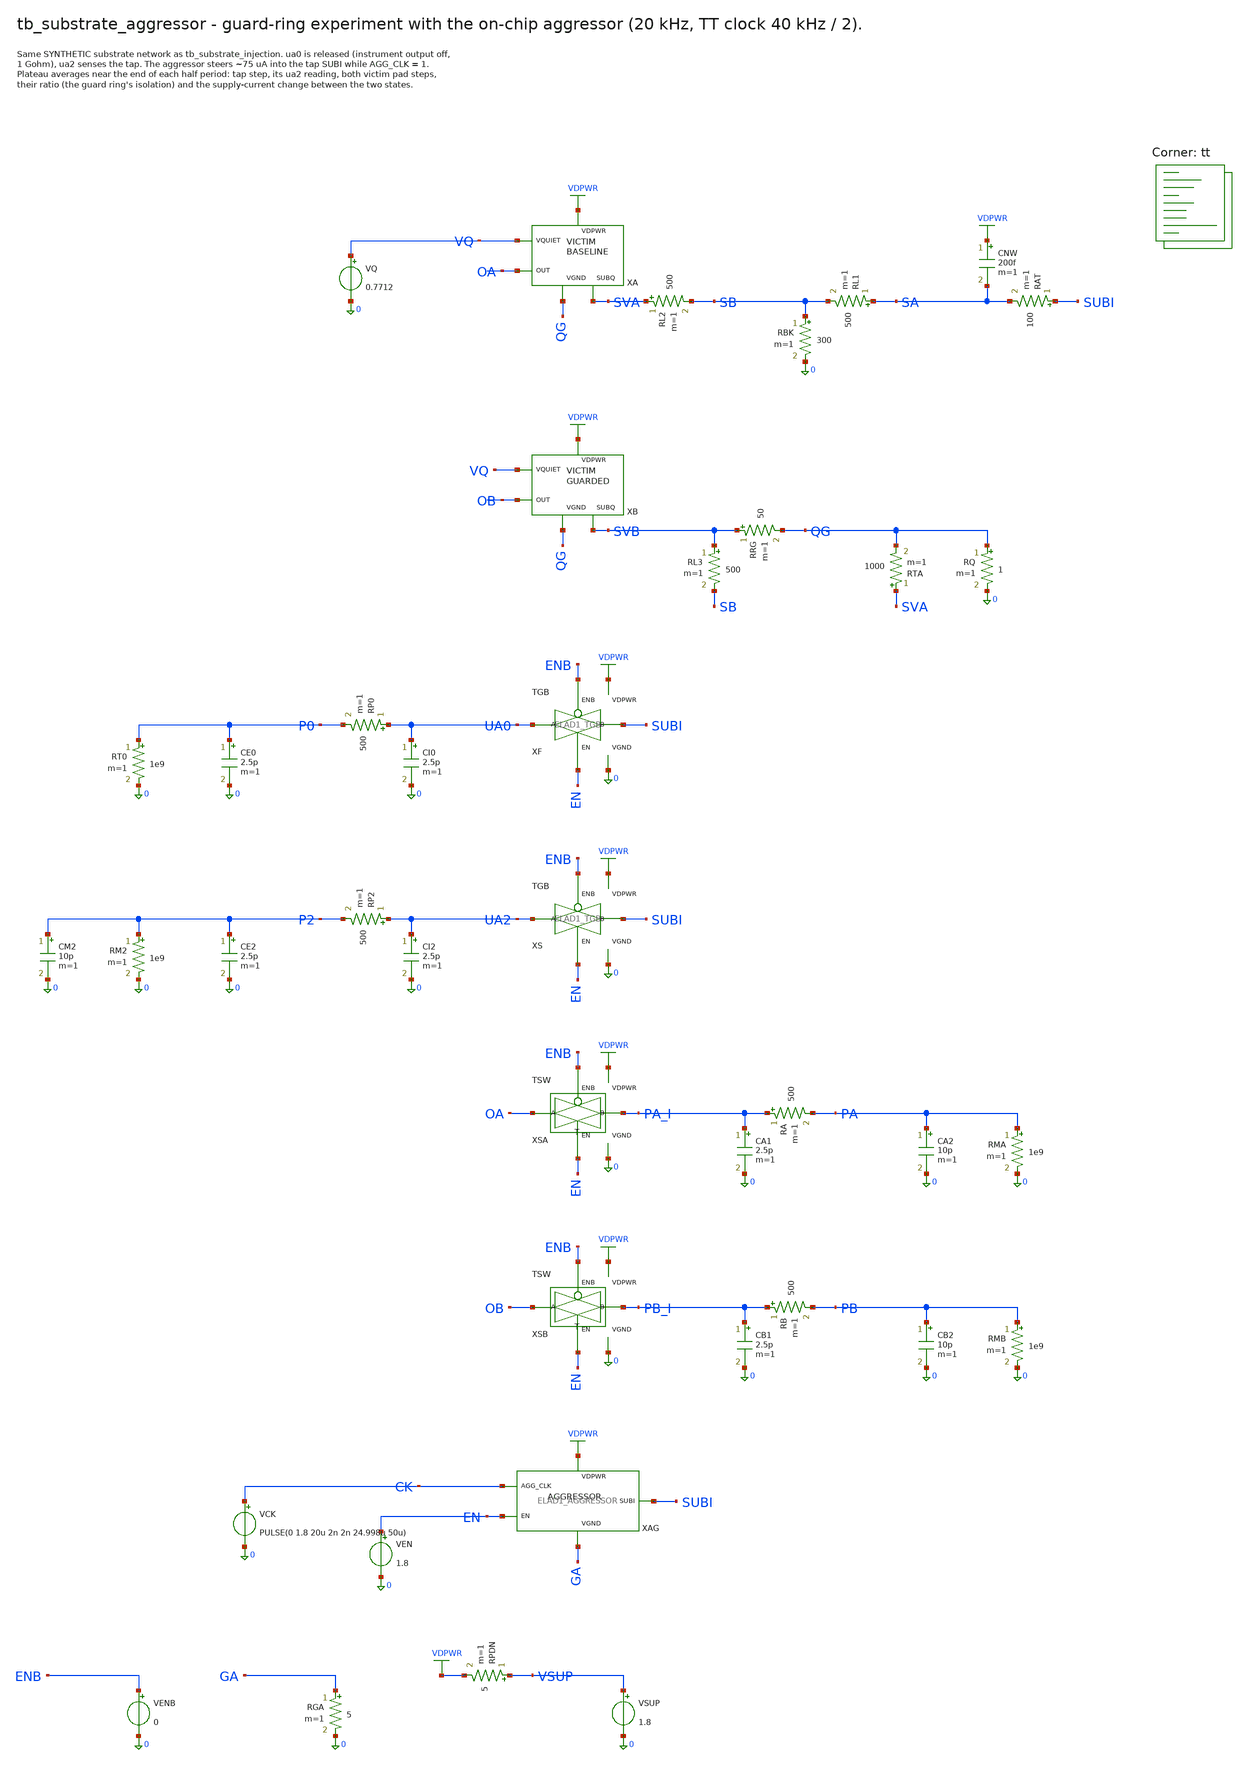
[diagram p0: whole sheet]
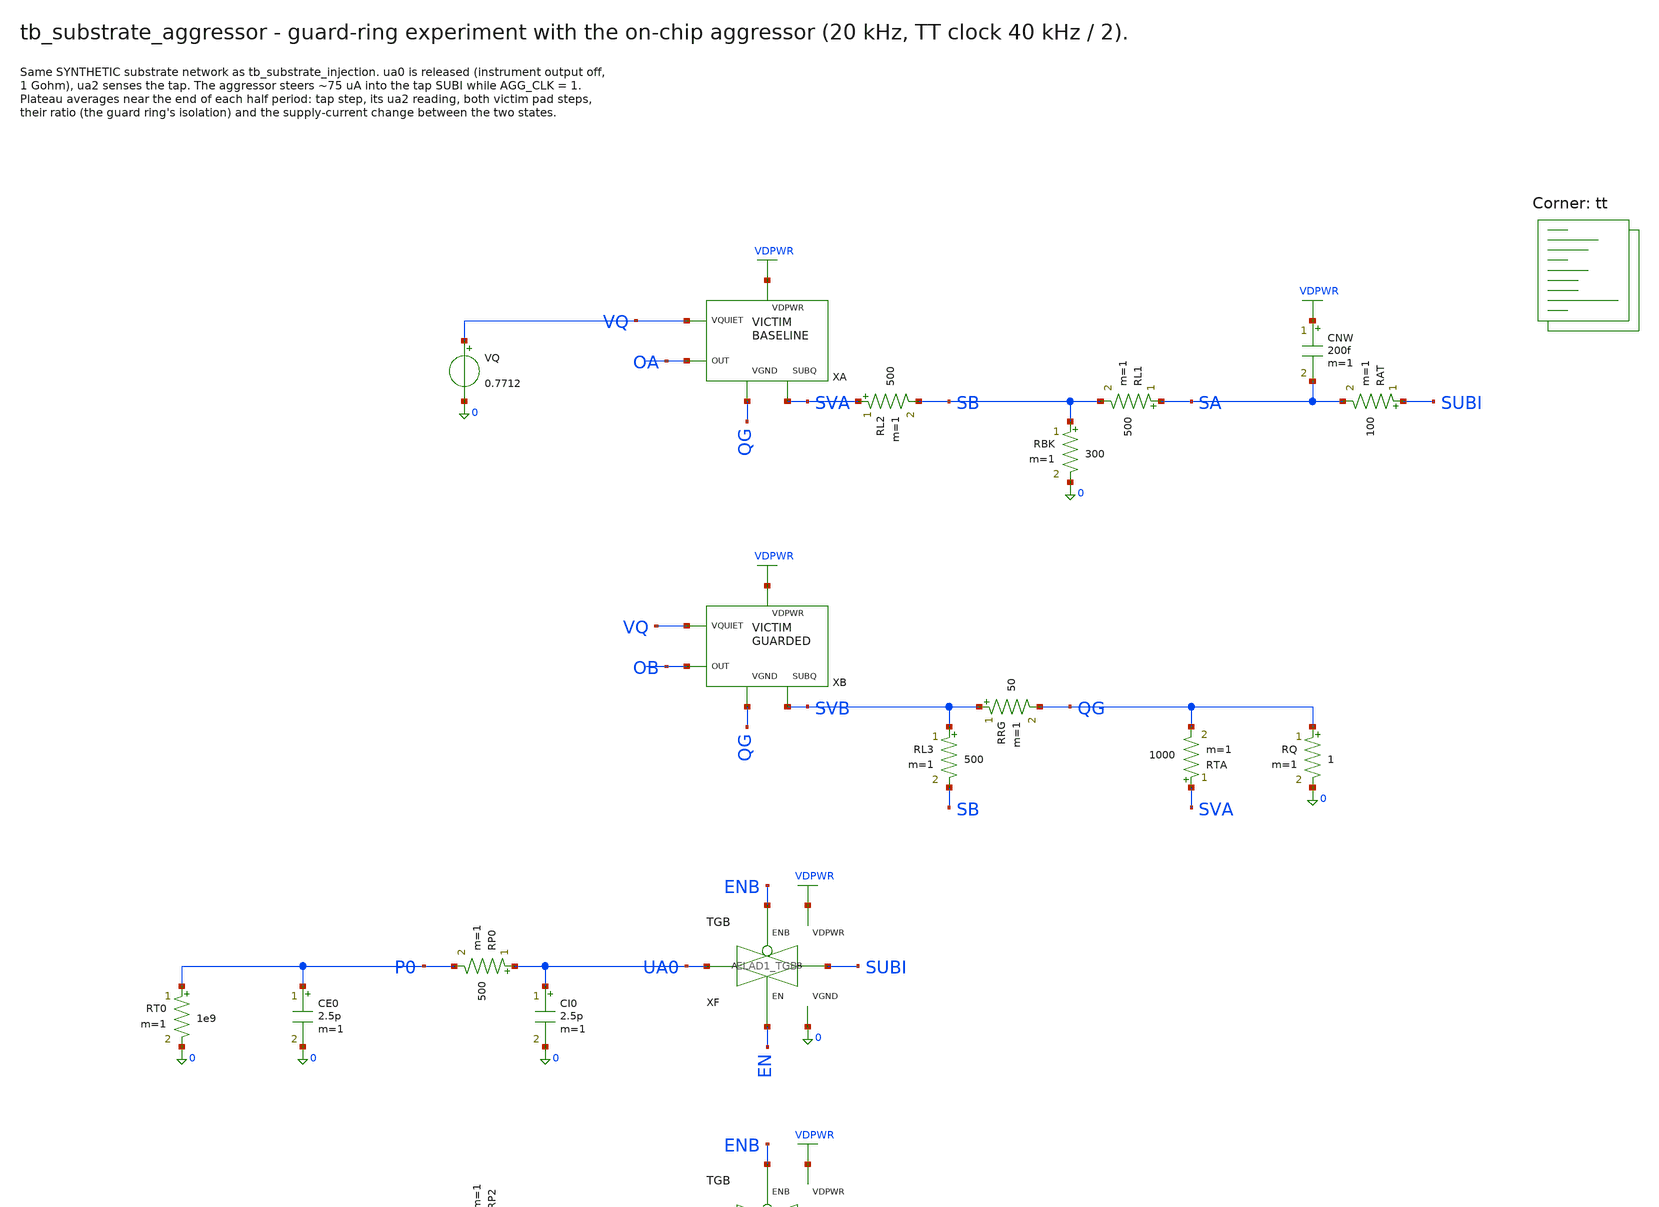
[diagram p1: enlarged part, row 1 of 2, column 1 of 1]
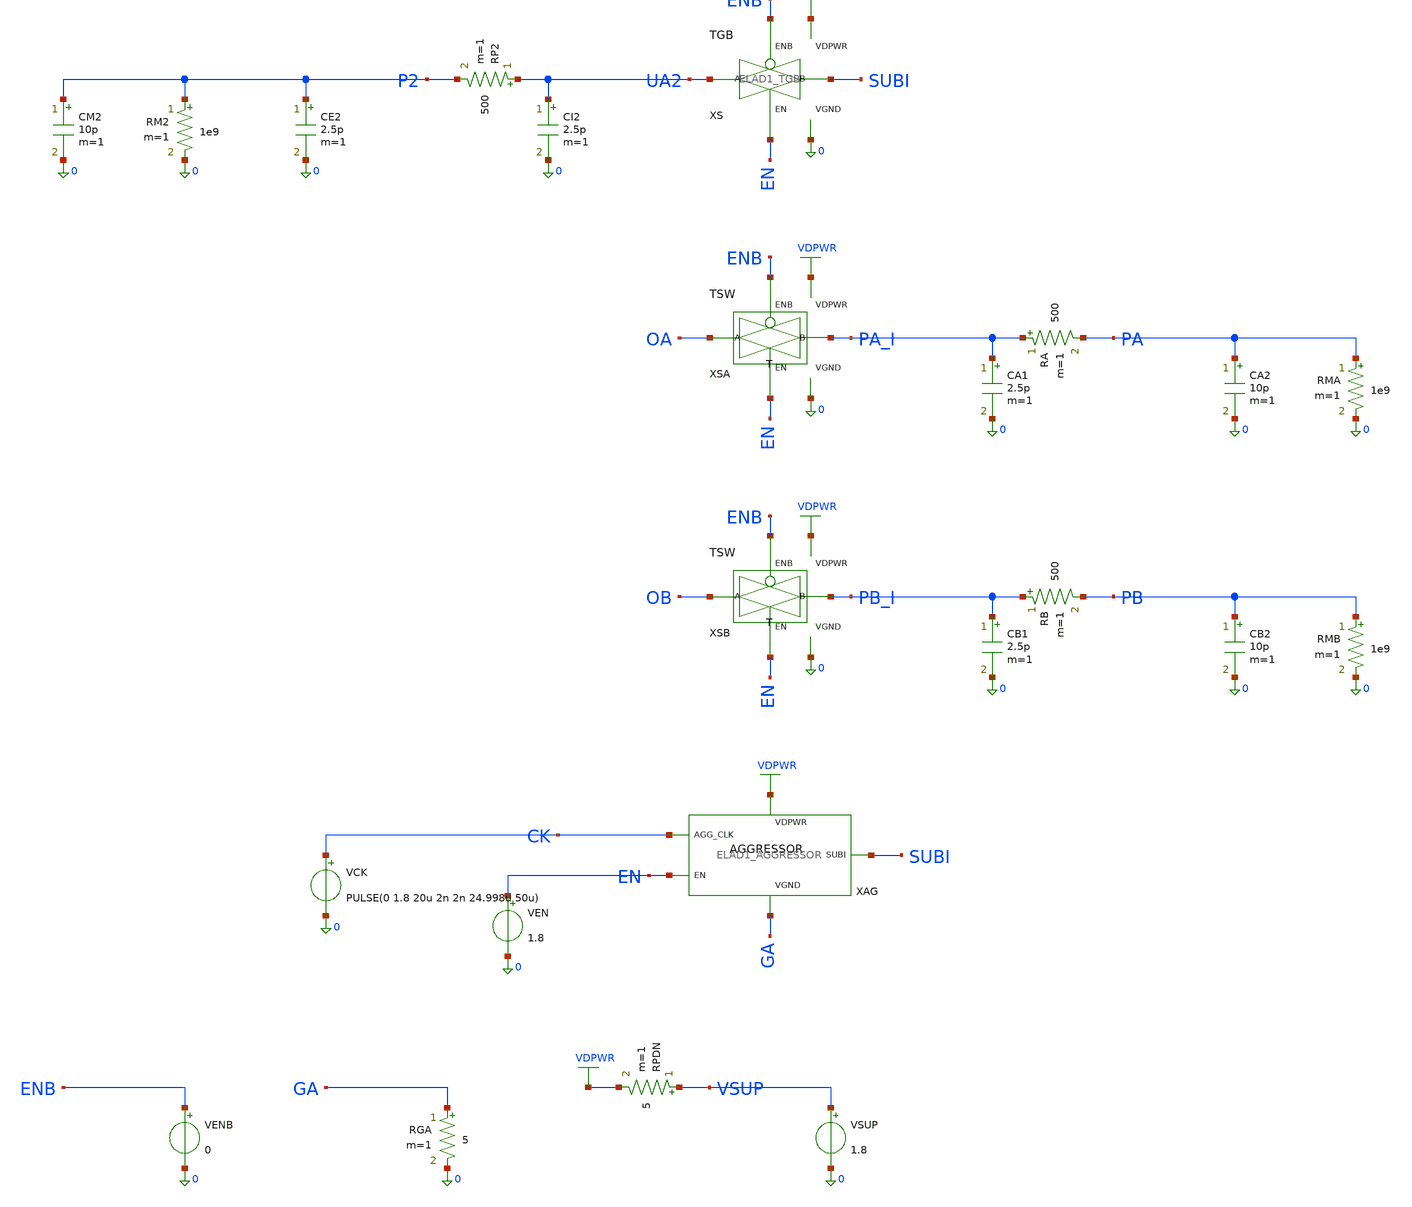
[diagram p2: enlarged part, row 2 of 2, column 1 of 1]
** sch_path: cells/ELAD1_AGGRESSOR/schematic/tb_substrate_aggressor.sch
**.subckt tb_substrate_aggressor
XA VQ OA VDPWR QG SVA ELAD1_VICTIM_BASELINE
VQ VQ 0 0.7712
RL2 SVA SB 500 m=1
RBK SB 0 300 m=1
RL1 SA SB 500 m=1
CNW VDPWR SA 200f m=1
RAT SUBI SA 100 m=1
XB VQ OB VDPWR QG SVB ELAD1_VICTIM_GUARDED
RL3 SVB SB 500 m=1
RRG SVB QG 50 m=1
RTA SVA QG 1000 m=1
RQ QG 0 1 m=1
XF UA0 SUBI EN ENB VDPWR 0 ELAD1_TGB
CI0 UA0 0 2.5p m=1
RP0 UA0 P0 500 m=1
CE0 P0 0 2.5p m=1
RT0 P0 0 1e9 m=1
XS UA2 SUBI EN ENB VDPWR 0 ELAD1_TGB
CI2 UA2 0 2.5p m=1
RP2 UA2 P2 500 m=1
CE2 P2 0 2.5p m=1
RM2 P2 0 1e9 m=1
CM2 P2 0 10p m=1
XSA OA PA_I EN ENB VDPWR 0 ELAD1_TSW
CA1 PA_I 0 2.5p m=1
RA PA_I PA 500 m=1
CA2 PA 0 10p m=1
RMA PA 0 1e9 m=1
XSB OB PB_I EN ENB VDPWR 0 ELAD1_TSW
CB1 PB_I 0 2.5p m=1
RB PB_I PB 500 m=1
CB2 PB 0 10p m=1
RMB PB 0 1e9 m=1
XAG CK EN VDPWR GA SUBI ELAD1_AGGRESSOR
VEN EN 0 1.8
VCK CK 0 PULSE(0 1.8 20u 2n 2n 24.998u 50u)
VENB ENB 0 0
RGA GA 0 5 m=1
RPDN VSUP VDPWR 5 m=1
VSUP VSUP 0 1.8
**** begin user architecture code

.option gmin=1e-15 reltol=1e-5 abstol=1e-14 vntol=1e-8 method=gear
.tran 20n 170u
.control
run
let isup = -i(VSUP)
meas tran sh avg v(SUBI) from=130u to=134.9u
meas tran sl avg v(SUBI) from=155u to=159.9u
meas tran p2h avg v(P2) from=130u to=134.9u
meas tran p2l avg v(P2) from=155u to=159.9u
meas tran pah avg v(PA) from=130u to=134.9u
meas tran pal avg v(PA) from=155u to=159.9u
meas tran pbh avg v(PB) from=130u to=134.9u
meas tran pbl avg v(PB) from=155u to=159.9u
meas tran ih avg isup from=130u to=134.9u
meas tran il avg isup from=155u to=159.9u
let tap_step = sh-sl
let sense_step = p2h-p2l
let pad_a = pah-pal
let pad_b = pbh-pbl
let ratio = pad_a/pad_b
let i_step_pct = 100*(ih-il)/il
echo ROW aggr tap_step=$&tap_step sense_step=$&sense_step pad_a=$&pad_a pad_b=$&pad_b ratio=$&ratio
+ i_step_pct=$&i_step_pct
.endc

.lib $::SKYWATER_MODELS/sky130.lib.spice tt
**** end user architecture code
**.ends

* expanding   symbol:  ELAD1_VICTIM_BASELINE.sym # of pins=5
** sym_path: cells/ELAD1_VICTIM_BASELINE/schematic/ELAD1_VICTIM_BASELINE.sym
** sch_path: cells/ELAD1_VICTIM_BASELINE/schematic/ELAD1_VICTIM_BASELINE.sch
.subckt ELAD1_VICTIM_BASELINE VQUIET OUT VDPWR VGND SUBQ
*.iopin VQUIET
*.iopin OUT
*.iopin VDPWR
*.iopin VGND
*.iopin SUBQ
XMVIC[1] OUT VQUIET VGND SUBQ sky130_fd_pr__nfet_01v8 L=1 W=1 nf=1 ad='int((1 + 1)/2) * 1 / 1 * 0.29'
+ as='int((1 + 2)/2) * 1 / 1 * 0.29' pd='2*int((1 + 1)/2) * (1 / 1 + 0.29)' ps='2*int((1 + 2)/2) * (1 / 1 + 0.29)'
+ nrd='0.29 / 1 ' nrs='0.29 / 1 ' sa=0 sb=0 sd=0 mult=1 m=1
XMVIC[0] OUT VQUIET VGND SUBQ sky130_fd_pr__nfet_01v8 L=1 W=1 nf=1 ad='int((1 + 1)/2) * 1 / 1 * 0.29'
+ as='int((1 + 2)/2) * 1 / 1 * 0.29' pd='2*int((1 + 1)/2) * (1 / 1 + 0.29)' ps='2*int((1 + 2)/2) * (1 / 1 + 0.29)'
+ nrd='0.29 / 1 ' nrs='0.29 / 1 ' sa=0 sb=0 sd=0 mult=1 m=1
XMD[1] VGND VGND VGND SUBQ sky130_fd_pr__nfet_01v8 L=1 W=1 nf=1 ad='int((1 + 1)/2) * 1 / 1 * 0.29' as='int((1 + 2)/2) * 1 / 1 * 0.29'
+ pd='2*int((1 + 1)/2) * (1 / 1 + 0.29)' ps='2*int((1 + 2)/2) * (1 / 1 + 0.29)' nrd='0.29 / 1 ' nrs='0.29 / 1 '
+ sa=0 sb=0 sd=0 mult=2 m=2
XMD[0] VGND VGND VGND SUBQ sky130_fd_pr__nfet_01v8 L=1 W=1 nf=1 ad='int((1 + 1)/2) * 1 / 1 * 0.29' as='int((1 + 2)/2) * 1 / 1 * 0.29'
+ pd='2*int((1 + 1)/2) * (1 / 1 + 0.29)' ps='2*int((1 + 2)/2) * (1 / 1 + 0.29)' nrd='0.29 / 1 ' nrs='0.29 / 1 '
+ sa=0 sb=0 sd=0 mult=2 m=2
XR1 OUT VDPWR SUBQ sky130_fd_pr__res_xhigh_po_0p69 L=31.7 mult=1 m=1
.ends


* expanding   symbol:  ELAD1_VICTIM_GUARDED.sym # of pins=5
** sym_path: cells/ELAD1_VICTIM_GUARDED/schematic/ELAD1_VICTIM_GUARDED.sym
** sch_path: cells/ELAD1_VICTIM_GUARDED/schematic/ELAD1_VICTIM_GUARDED.sch
.subckt ELAD1_VICTIM_GUARDED VQUIET OUT VDPWR VGND SUBQ
*.iopin VQUIET
*.iopin OUT
*.iopin VDPWR
*.iopin VGND
*.iopin SUBQ
XRLD VDPWR OUT SUBQ sky130_fd_pr__res_xhigh_po W=0.69 L=31.7 mult=1 m=1
XMVIC OUT VQUIET VGND SUBQ sky130_fd_pr__nfet_01v8 L=1 W=2 nf=1 ad='int((1 + 1)/2) * 2 / 1 * 0.29' as='int((1 + 2)/2) * 2 / 1 * 0.29'
+ pd='2*int((1 + 1)/2) * (2 / 1 + 0.29)' ps='2*int((1 + 2)/2) * (2 / 1 + 0.29)' nrd='0.29 / 2 ' nrs='0.29 / 2 '
+ sa=0 sb=0 sd=0 mult=1 m=1
XDUM[1] VGND VGND VGND SUBQ sky130_fd_pr__nfet_01v8 L=1 W=2 nf=1 ad='int((1 + 1)/2) * 2 / 1 * 0.29' as='int((1 + 2)/2) * 2 / 1 * 0.29'
+ pd='2*int((1 + 1)/2) * (2 / 1 + 0.29)' ps='2*int((1 + 2)/2) * (2 / 1 + 0.29)' nrd='0.29 / 2 ' nrs='0.29 / 2 '
+ sa=0 sb=0 sd=0 mult=1 m=1
XDUM[0] VGND VGND VGND SUBQ sky130_fd_pr__nfet_01v8 L=1 W=2 nf=1 ad='int((1 + 1)/2) * 2 / 1 * 0.29' as='int((1 + 2)/2) * 2 / 1 * 0.29'
+ pd='2*int((1 + 1)/2) * (2 / 1 + 0.29)' ps='2*int((1 + 2)/2) * (2 / 1 + 0.29)' nrd='0.29 / 2 ' nrs='0.29 / 2 '
+ sa=0 sb=0 sd=0 mult=1 m=1
.ends


* expanding   symbol:  ELAD1_TGB.sym # of pins=6
** sym_path: cells/ELAD1_TGB/schematic/ELAD1_TGB.sym
** sch_path: cells/ELAD1_TGB/schematic/ELAD1_TGB.sch
.subckt ELAD1_TGB A B EN ENB VDPWR VGND
*.iopin A
*.iopin B
*.iopin EN
*.iopin ENB
*.iopin VDPWR
*.iopin VGND
XMN A EN B VGND sky130_fd_pr__nfet_01v8 L=0.15 W=1 nf=1 ad='int((1 + 1)/2) * 1 / 1 * 0.29' as='int((1 + 2)/2) * 1 / 1 * 0.29'
+ pd='2*int((1 + 1)/2) * (1 / 1 + 0.29)' ps='2*int((1 + 2)/2) * (1 / 1 + 0.29)' nrd='0.29 / 1 ' nrs='0.29 / 1 '
+ sa=0 sb=0 sd=0 mult=1 m=1
XMP A ENB B VDPWR sky130_fd_pr__pfet_01v8 L=0.15 W=2 nf=1 ad='int((nf+1)/2) * W/nf * 0.29' as='int((nf+2)/2) * W/nf * 0.29'
+ pd='2*int((nf+1)/2) * (W/nf + 0.29)' ps='2*int((nf+2)/2) * (W/nf + 0.29)' nrd='0.29 / W' nrs='0.29 / W'
+ sa=0 sb=0 sd=0 mult=1 m=1
.ends


* expanding   symbol:  ELAD1_TSW.sym # of pins=6
** sym_path: cells/ELAD1_TSW/schematic/ELAD1_TSW.sym
** sch_path: cells/ELAD1_TSW/schematic/ELAD1_TSW.sch
.subckt ELAD1_TSW A B EN ENB VDPWR VGND
*.iopin A
*.iopin B
*.iopin EN
*.iopin ENB
*.iopin VDPWR
*.iopin VGND
x1 A M EN ENB VDPWR VGND ELAD1_TGA
x1 M B EN ENB VDPWR VGND ELAD1_TGA
XMN1 M ENB VGND VGND sky130_fd_pr__nfet_01v8 L=0.15 W=1 nf=1 ad='int((1 + 1)/2) * 1 / 1 * 0.29' as='int((1 + 2)/2) * 1 / 1 * 0.29'
+ pd='2*int((1 + 1)/2) * (1 / 1 + 0.29)' ps='2*int((1 + 2)/2) * (1 / 1 + 0.29)' nrd='0.29 / 1 ' nrs='0.29 / 1 '
+ sa=0 sb=0 sd=0 mult=1 m=1
.ends


* expanding   symbol:  ELAD1_AGGRESSOR.sym # of pins=5
** sym_path: cells/ELAD1_AGGRESSOR/schematic/ELAD1_AGGRESSOR.sym
** sch_path: cells/ELAD1_AGGRESSOR/schematic/ELAD1_AGGRESSOR.sch
.subckt ELAD1_AGGRESSOR AGG_CLK EN VDPWR VGND SUBI
*.iopin AGG_CLK
*.iopin EN
*.iopin VDPWR
*.iopin VGND
*.iopin SUBI
XIC AGG_CLK CKB VDPWR VGND ELAD1_INV
XIE EN ENB VDPWR VGND ELAD1_INV
XGIP1 gip ENB VDPWR VDPWR sky130_fd_pr__pfet_01v8 L=0.15 W=2 nf=1 ad='int((nf+1)/2) * W/nf * 0.29' as='int((nf+2)/2) * W/nf * 0.29'
+ pd='2*int((nf+1)/2) * (W/nf + 0.29)' ps='2*int((nf+2)/2) * (W/nf + 0.29)' nrd='0.29 / W' nrs='0.29 / W'
+ sa=0 sb=0 sd=0 mult=1 m=1
XGIP2 GI CKB gip VDPWR sky130_fd_pr__pfet_01v8 L=0.15 W=2 nf=1 ad='int((nf+1)/2) * W/nf * 0.29' as='int((nf+2)/2) * W/nf * 0.29'
+ pd='2*int((nf+1)/2) * (W/nf + 0.29)' ps='2*int((nf+2)/2) * (W/nf + 0.29)' nrd='0.29 / W' nrs='0.29 / W'
+ sa=0 sb=0 sd=0 mult=1 m=1
XGIN1 GI ENB VGND VGND sky130_fd_pr__nfet_01v8 L=1 W=0.42 nf=1 ad='int((1 + 1)/2) * 0.42 / 1 * 0.29'
+ as='int((1 + 2)/2) * 0.42 / 1 * 0.29' pd='2*int((1 + 1)/2) * (0.42 / 1 + 0.29)' ps='2*int((1 + 2)/2) * (0.42 / 1 + 0.29)'
+ nrd='0.29 / 0.42 ' nrs='0.29 / 0.42 ' sa=0 sb=0 sd=0 mult=1 m=1
XGIN2 GI CKB VGND VGND sky130_fd_pr__nfet_01v8 L=1 W=0.42 nf=1 ad='int((1 + 1)/2) * 0.42 / 1 * 0.29'
+ as='int((1 + 2)/2) * 0.42 / 1 * 0.29' pd='2*int((1 + 1)/2) * (0.42 / 1 + 0.29)' ps='2*int((1 + 2)/2) * (0.42 / 1 + 0.29)'
+ nrd='0.29 / 0.42 ' nrs='0.29 / 0.42 ' sa=0 sb=0 sd=0 mult=1 m=1
XGDP1 gdp ENB VDPWR VDPWR sky130_fd_pr__pfet_01v8 L=0.15 W=2 nf=1 ad='int((nf+1)/2) * W/nf * 0.29' as='int((nf+2)/2) * W/nf * 0.29'
+ pd='2*int((nf+1)/2) * (W/nf + 0.29)' ps='2*int((nf+2)/2) * (W/nf + 0.29)' nrd='0.29 / W' nrs='0.29 / W'
+ sa=0 sb=0 sd=0 mult=1 m=1
XGDP2 GD AGG_CLK gdp VDPWR sky130_fd_pr__pfet_01v8 L=0.15 W=2 nf=1 ad='int((nf+1)/2) * W/nf * 0.29' as='int((nf+2)/2) * W/nf * 0.29'
+ pd='2*int((nf+1)/2) * (W/nf + 0.29)' ps='2*int((nf+2)/2) * (W/nf + 0.29)' nrd='0.29 / W' nrs='0.29 / W'
+ sa=0 sb=0 sd=0 mult=1 m=1
XGDN1 GD ENB VGND VGND sky130_fd_pr__nfet_01v8 L=1 W=0.42 nf=1 ad='int((1 + 1)/2) * 0.42 / 1 * 0.29'
+ as='int((1 + 2)/2) * 0.42 / 1 * 0.29' pd='2*int((1 + 1)/2) * (0.42 / 1 + 0.29)' ps='2*int((1 + 2)/2) * (0.42 / 1 + 0.29)'
+ nrd='0.29 / 0.42 ' nrs='0.29 / 0.42 ' sa=0 sb=0 sd=0 mult=1 m=1
XGDN2 GD AGG_CLK VGND VGND sky130_fd_pr__nfet_01v8 L=1 W=0.42 nf=1 ad='int((1 + 1)/2) * 0.42 / 1 * 0.29'
+ as='int((1 + 2)/2) * 0.42 / 1 * 0.29' pd='2*int((1 + 1)/2) * (0.42 / 1 + 0.29)' ps='2*int((1 + 2)/2) * (0.42 / 1 + 0.29)'
+ nrd='0.29 / 0.42 ' nrs='0.29 / 0.42 ' sa=0 sb=0 sd=0 mult=1 m=1
XRL X VDPWR VGND sky130_fd_pr__res_xhigh_po W=0.69 L=7.3 mult=1 m=1
XMINJ X GI SUBI VGND sky130_fd_pr__nfet_01v8 L=0.15 W=2 nf=1 ad='int((1 + 1)/2) * 2 / 1 * 0.29' as='int((1 + 2)/2) * 2 / 1 * 0.29'
+ pd='2*int((1 + 1)/2) * (2 / 1 + 0.29)' ps='2*int((1 + 2)/2) * (2 / 1 + 0.29)' nrd='0.29 / 2 ' nrs='0.29 / 2 '
+ sa=0 sb=0 sd=0 mult=1 m=1
XMDUM X GD D VGND sky130_fd_pr__nfet_01v8 L=0.15 W=2 nf=1 ad='int((1 + 1)/2) * 2 / 1 * 0.29' as='int((1 + 2)/2) * 2 / 1 * 0.29'
+ pd='2*int((1 + 1)/2) * (2 / 1 + 0.29)' ps='2*int((1 + 2)/2) * (2 / 1 + 0.29)' nrd='0.29 / 2 ' nrs='0.29 / 2 '
+ sa=0 sb=0 sd=0 mult=1 m=1
XRDUM VGND D sky130_fd_pr__res_generic_po W=1 L=15 m=1
.ends


* expanding   symbol:  ELAD1_TGA.sym # of pins=6
** sym_path: cells/ELAD1_TGA/schematic/ELAD1_TGA.sym
** sch_path: cells/ELAD1_TGA/schematic/ELAD1_TGA.sch
.subckt ELAD1_TGA A B EN ENB VDPWR VGND
*.iopin A
*.iopin B
*.iopin EN
*.iopin ENB
*.iopin VDPWR
*.iopin VGND
XMN A EN B VGND sky130_fd_pr__nfet_01v8_lvt L=0.15 W=4 nf=1 ad='int((1 + 1)/2) * 4 / 1 * 0.29' as='int((1 + 2)/2) * 4 / 1 * 0.29'
+ pd='2*int((1 + 1)/2) * (4 / 1 + 0.29)' ps='2*int((1 + 2)/2) * (4 / 1 + 0.29)' nrd='0.29 / 4 ' nrs='0.29 / 4 '
+ sa=0 sb=0 sd=0 mult=1 m=1
XMP A ENB B VDPWR sky130_fd_pr__pfet_01v8_lvt L=0.35 W=12 nf=1 ad='int((1 + 1)/2) * 12 / 1 * 0.29' as='int((1 + 2)/2) * 12 / 1 * 0.29'
+ pd='2*int((1 + 1)/2) * (12 / 1 + 0.29)' ps='2*int((1 + 2)/2) * (12 / 1 + 0.29)' nrd='0.29 / 12 ' nrs='0.29 / 12 '
+ sa=0 sb=0 sd=0 mult=1 m=1
.ends


* expanding   symbol:  ELAD1_INV.sym # of pins=4
** sym_path: cells/ELAD1_INV/schematic/ELAD1_INV.sym
** sch_path: cells/ELAD1_INV/schematic/ELAD1_INV.sch
.subckt ELAD1_INV A Y VDPWR VGND
*.iopin A
*.iopin Y
*.iopin VDPWR
*.iopin VGND
XMN Y A VGND VGND sky130_fd_pr__nfet_01v8 L=0.15 W=0.65 nf=1 ad='int((1 + 1)/2) * 0.65 / 1 * 0.29' as='int((1 + 2)/2) * 0.65 / 1 * 0.29'
+ pd='2*int((1 + 1)/2) * (0.65 / 1 + 0.29)' ps='2*int((1 + 2)/2) * (0.65 / 1 + 0.29)' nrd='0.29 / 0.65 '
+ nrs='0.29 / 0.65 ' sa=0 sb=0 sd=0 mult=1 m=1
XMP Y A VDPWR VDPWR sky130_fd_pr__pfet_01v8 L=0.15 W=1 nf=1 ad='int((nf+1)/2) * W/nf * 0.29' as='int((nf+2)/2) * W/nf * 0.29'
+ pd='2*int((nf+1)/2) * (W/nf + 0.29)' ps='2*int((nf+2)/2) * (W/nf + 0.29)' nrd='0.29 / W' nrs='0.29 / W'
+ sa=0 sb=0 sd=0 mult=1 m=1
.ends

.GLOBAL VGND
.GLOBAL VDPWR
.end
